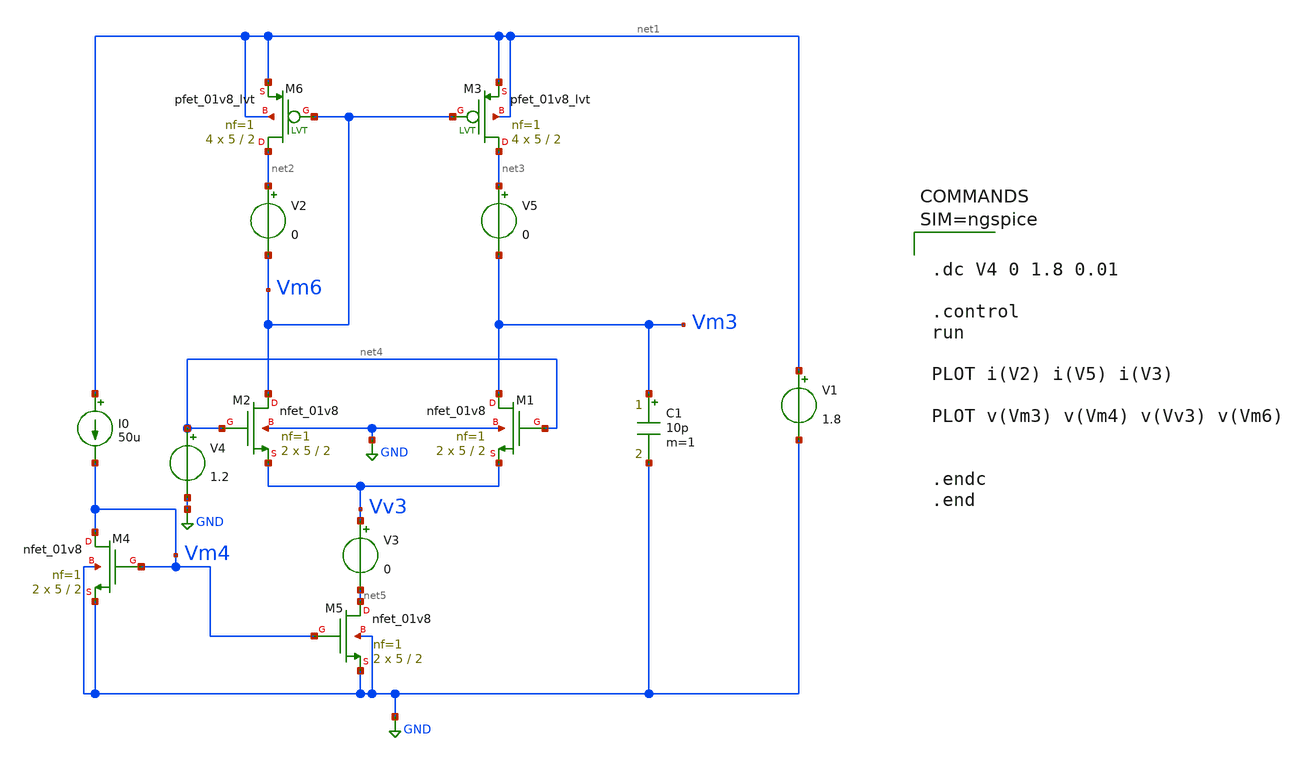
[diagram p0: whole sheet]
** sch_path: sch/Diff_Amplifier.sch
**.subckt Diff_Amplifier
XM2 Vm6 net4 Vv3 GND sky130_fd_pr__nfet_01v8 L=2 W=5 nf=1 ad='int((1 + 1)/2) * 5 / 1 * 0.29' as='int((1 + 2)/2) * 5 / 1 * 0.29'
+ pd='2*int((1 + 1)/2) * (5 / 1 + 0.29)' ps='2*int((1 + 2)/2) * (5 / 1 + 0.29)' nrd='0.29 / 5 ' nrs='0.29 / 5 '
+ sa=0 sb=0 sd=0 mult=2 m=2
XM1 Vm3 net4 Vv3 GND sky130_fd_pr__nfet_01v8 L=2 W=5 nf=1 ad='int((1 + 1)/2) * 5 / 1 * 0.29' as='int((1 + 2)/2) * 5 / 1 * 0.29'
+ pd='2*int((1 + 1)/2) * (5 / 1 + 0.29)' ps='2*int((1 + 2)/2) * (5 / 1 + 0.29)' nrd='0.29 / 5 ' nrs='0.29 / 5 '
+ sa=0 sb=0 sd=0 mult=2 m=2
XM6 net2 Vm6 net1 net1 sky130_fd_pr__pfet_01v8_lvt L=2 W=5 nf=1 ad='int((1 + 1)/2) * 5 / 1 * 0.29' as='int((1 + 2)/2) * 5 / 1 * 0.29'
+ pd='2*int((1 + 1)/2) * (5 / 1 + 0.29)' ps='2*int((1 + 2)/2) * (5 / 1 + 0.29)' nrd='0.29 / 5 ' nrs='0.29 / 5 '
+ sa=0 sb=0 sd=0 mult=4 m=4
XM3 net3 Vm6 net1 net1 sky130_fd_pr__pfet_01v8_lvt L=2 W=5 nf=1 ad='int((1 + 1)/2) * 5 / 1 * 0.29' as='int((1 + 2)/2) * 5 / 1 * 0.29'
+ pd='2*int((1 + 1)/2) * (5 / 1 + 0.29)' ps='2*int((1 + 2)/2) * (5 / 1 + 0.29)' nrd='0.29 / 5 ' nrs='0.29 / 5 '
+ sa=0 sb=0 sd=0 mult=4 m=4
XM4 Vm4 Vm4 GND GND sky130_fd_pr__nfet_01v8 L=2 W=5 nf=1 ad='int((1 + 1)/2) * 5 / 1 * 0.29' as='int((1 + 2)/2) * 5 / 1 * 0.29'
+ pd='2*int((1 + 1)/2) * (5 / 1 + 0.29)' ps='2*int((1 + 2)/2) * (5 / 1 + 0.29)' nrd='0.29 / 5 ' nrs='0.29 / 5 '
+ sa=0 sb=0 sd=0 mult=2 m=2
XM5 net5 Vm4 GND GND sky130_fd_pr__nfet_01v8 L=2 W=5 nf=1 ad='int((1 + 1)/2) * 5 / 1 * 0.29' as='int((1 + 2)/2) * 5 / 1 * 0.29'
+ pd='2*int((1 + 1)/2) * (5 / 1 + 0.29)' ps='2*int((1 + 2)/2) * (5 / 1 + 0.29)' nrd='0.29 / 5 ' nrs='0.29 / 5 '
+ sa=0 sb=0 sd=0 mult=2 m=2
I0 net1 Vm4 50u
C1 Vm3 GND 10p m=1
V1 net1 GND 1.8
V2 net2 Vm6 0
V3 Vv3 net5 0
V5 net3 Vm3 0
V4 net4 GND 1.2
**** begin user architecture code

** opencircuitdesign pdks install
.lib $::SKYWATER_MODELS/sky130.lib.spice tt




.dc V4 0 1.8 0.01

.control
run

PLOT i(V2) i(V5) i(V3)

PLOT v(Vm3) v(Vm4) v(Vv3) v(Vm6)


.endc
.end



**** end user architecture code
**.ends
.GLOBAL GND
.end
